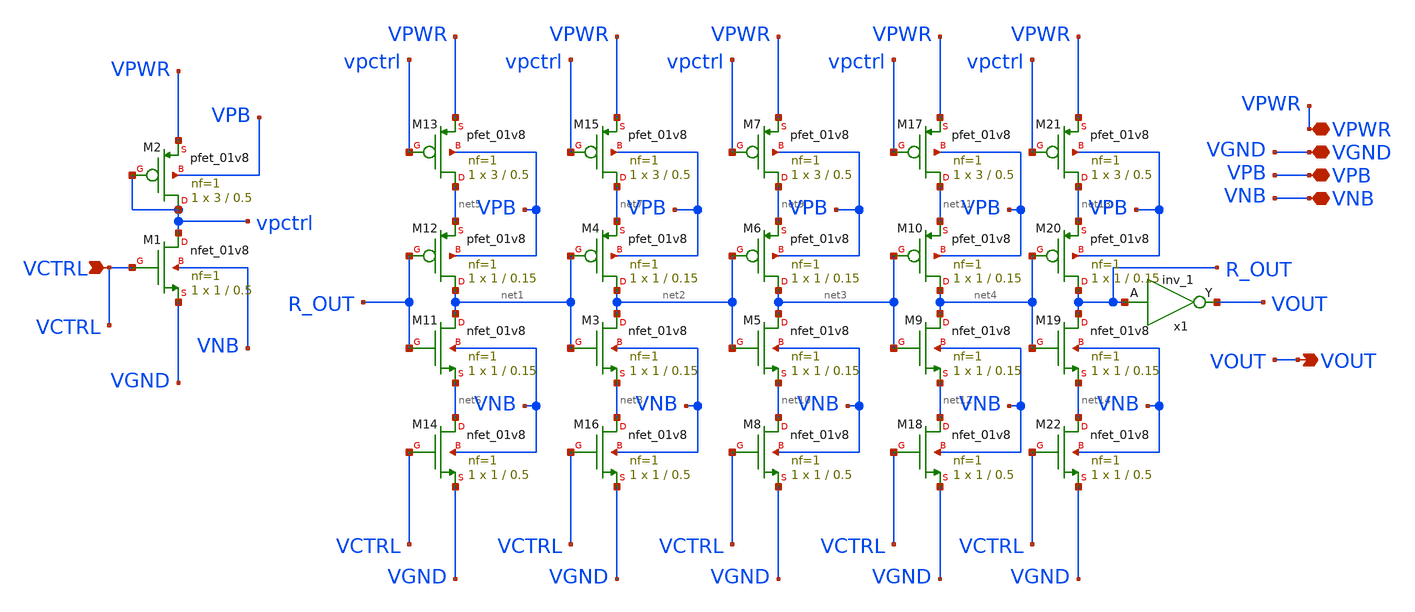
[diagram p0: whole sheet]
** sch_path: vco.sch
**.subckt vco VPWR VGND VPB VNB VOUT VCTRL
*.iopin VPWR
*.iopin VGND
*.iopin VPB
*.iopin VNB
*.opin VOUT
*.ipin VCTRL
XM1 vpctrl VCTRL VGND VNB sky130_fd_pr__nfet_01v8 L=0.5 W=1 nf=1 ad='int((1 + 1)/2) * 1 / 1 * 0.29' as='int((1 + 2)/2) * 1 / 1 * 0.29'
+ pd='2*int((1 + 1)/2) * (1 / 1 + 0.29)' ps='2*int((1 + 2)/2) * (1 / 1 + 0.29)' nrd='0.29 / 1 ' nrs='0.29 / 1 '
+ sa=0 sb=0 sd=0 mult=1 m=1
XM2 vpctrl vpctrl VPWR VPB sky130_fd_pr__pfet_01v8 L=0.5 W=3 nf=1 ad='int((1 + 1)/2) * 3 / 1 * 0.29'
+ as='int((1 + 2)/2) * 3 / 1 * 0.29' pd='2*int((1 + 1)/2) * (3 / 1 + 0.29)' ps='2*int((1 + 2)/2) * (3 / 1 + 0.29)'
+ nrd='0.29 / 3 ' nrs='0.29 / 3 ' sa=0 sb=0 sd=0 mult=1 m=1
XM11 net1 R_OUT net6 VNB sky130_fd_pr__nfet_01v8 L=0.15 W=1 nf=1 ad='int((1 + 1)/2) * 1 / 1 * 0.29' as='int((1 + 2)/2) * 1 / 1 * 0.29'
+ pd='2*int((1 + 1)/2) * (1 / 1 + 0.29)' ps='2*int((1 + 2)/2) * (1 / 1 + 0.29)' nrd='0.29 / 1 ' nrs='0.29 / 1 '
+ sa=0 sb=0 sd=0 mult=1 m=1
XM12 net1 R_OUT net5 VPB sky130_fd_pr__pfet_01v8 L=0.15 W=1 nf=1 ad='int((1 + 1)/2) * 1 / 1 * 0.29' as='int((1 + 2)/2) * 1 / 1 * 0.29'
+ pd='2*int((1 + 1)/2) * (1 / 1 + 0.29)' ps='2*int((1 + 2)/2) * (1 / 1 + 0.29)' nrd='0.29 / 1 ' nrs='0.29 / 1 '
+ sa=0 sb=0 sd=0 mult=1 m=1
XM13 net5 vpctrl VPWR VPB sky130_fd_pr__pfet_01v8 L=0.5 W=3 nf=1 ad='int((1 + 1)/2) * 3 / 1 * 0.29' as='int((1 + 2)/2) * 3 / 1 * 0.29'
+ pd='2*int((1 + 1)/2) * (3 / 1 + 0.29)' ps='2*int((1 + 2)/2) * (3 / 1 + 0.29)' nrd='0.29 / 3 ' nrs='0.29 / 3 '
+ sa=0 sb=0 sd=0 mult=1 m=1
XM14 net6 VCTRL VGND VNB sky130_fd_pr__nfet_01v8 L=0.5 W=1 nf=1 ad='int((1 + 1)/2) * 1 / 1 * 0.29' as='int((1 + 2)/2) * 1 / 1 * 0.29'
+ pd='2*int((1 + 1)/2) * (1 / 1 + 0.29)' ps='2*int((1 + 2)/2) * (1 / 1 + 0.29)' nrd='0.29 / 1 ' nrs='0.29 / 1 '
+ sa=0 sb=0 sd=0 mult=1 m=1
XM3 net2 net1 net8 VNB sky130_fd_pr__nfet_01v8 L=0.15 W=1 nf=1 ad='int((1 + 1)/2) * 1 / 1 * 0.29' as='int((1 + 2)/2) * 1 / 1 * 0.29'
+ pd='2*int((1 + 1)/2) * (1 / 1 + 0.29)' ps='2*int((1 + 2)/2) * (1 / 1 + 0.29)' nrd='0.29 / 1 ' nrs='0.29 / 1 '
+ sa=0 sb=0 sd=0 mult=1 m=1
XM4 net2 net1 net7 VPB sky130_fd_pr__pfet_01v8 L=0.15 W=1 nf=1 ad='int((1 + 1)/2) * 1 / 1 * 0.29' as='int((1 + 2)/2) * 1 / 1 * 0.29'
+ pd='2*int((1 + 1)/2) * (1 / 1 + 0.29)' ps='2*int((1 + 2)/2) * (1 / 1 + 0.29)' nrd='0.29 / 1 ' nrs='0.29 / 1 '
+ sa=0 sb=0 sd=0 mult=1 m=1
XM15 net7 vpctrl VPWR VPB sky130_fd_pr__pfet_01v8 L=0.5 W=3 nf=1 ad='int((1 + 1)/2) * 3 / 1 * 0.29' as='int((1 + 2)/2) * 3 / 1 * 0.29'
+ pd='2*int((1 + 1)/2) * (3 / 1 + 0.29)' ps='2*int((1 + 2)/2) * (3 / 1 + 0.29)' nrd='0.29 / 3 ' nrs='0.29 / 3 '
+ sa=0 sb=0 sd=0 mult=1 m=1
XM16 net8 VCTRL VGND VNB sky130_fd_pr__nfet_01v8 L=0.5 W=1 nf=1 ad='int((1 + 1)/2) * 1 / 1 * 0.29' as='int((1 + 2)/2) * 1 / 1 * 0.29'
+ pd='2*int((1 + 1)/2) * (1 / 1 + 0.29)' ps='2*int((1 + 2)/2) * (1 / 1 + 0.29)' nrd='0.29 / 1 ' nrs='0.29 / 1 '
+ sa=0 sb=0 sd=0 mult=1 m=1
XM5 net3 net2 net10 VNB sky130_fd_pr__nfet_01v8 L=0.15 W=1 nf=1 ad='int((1 + 1)/2) * 1 / 1 * 0.29' as='int((1 + 2)/2) * 1 / 1 * 0.29'
+ pd='2*int((1 + 1)/2) * (1 / 1 + 0.29)' ps='2*int((1 + 2)/2) * (1 / 1 + 0.29)' nrd='0.29 / 1 ' nrs='0.29 / 1 '
+ sa=0 sb=0 sd=0 mult=1 m=1
XM6 net3 net2 net9 VPB sky130_fd_pr__pfet_01v8 L=0.15 W=1 nf=1 ad='int((1 + 1)/2) * 1 / 1 * 0.29' as='int((1 + 2)/2) * 1 / 1 * 0.29'
+ pd='2*int((1 + 1)/2) * (1 / 1 + 0.29)' ps='2*int((1 + 2)/2) * (1 / 1 + 0.29)' nrd='0.29 / 1 ' nrs='0.29 / 1 '
+ sa=0 sb=0 sd=0 mult=1 m=1
XM7 net9 vpctrl VPWR VPB sky130_fd_pr__pfet_01v8 L=0.5 W=3 nf=1 ad='int((1 + 1)/2) * 3 / 1 * 0.29' as='int((1 + 2)/2) * 3 / 1 * 0.29'
+ pd='2*int((1 + 1)/2) * (3 / 1 + 0.29)' ps='2*int((1 + 2)/2) * (3 / 1 + 0.29)' nrd='0.29 / 3 ' nrs='0.29 / 3 '
+ sa=0 sb=0 sd=0 mult=1 m=1
XM8 net10 VCTRL VGND VNB sky130_fd_pr__nfet_01v8 L=0.5 W=1 nf=1 ad='int((1 + 1)/2) * 1 / 1 * 0.29' as='int((1 + 2)/2) * 1 / 1 * 0.29'
+ pd='2*int((1 + 1)/2) * (1 / 1 + 0.29)' ps='2*int((1 + 2)/2) * (1 / 1 + 0.29)' nrd='0.29 / 1 ' nrs='0.29 / 1 '
+ sa=0 sb=0 sd=0 mult=1 m=1
XM9 net4 net3 net12 VNB sky130_fd_pr__nfet_01v8 L=0.15 W=1 nf=1 ad='int((1 + 1)/2) * 1 / 1 * 0.29' as='int((1 + 2)/2) * 1 / 1 * 0.29'
+ pd='2*int((1 + 1)/2) * (1 / 1 + 0.29)' ps='2*int((1 + 2)/2) * (1 / 1 + 0.29)' nrd='0.29 / 1 ' nrs='0.29 / 1 '
+ sa=0 sb=0 sd=0 mult=1 m=1
XM10 net4 net3 net11 VPB sky130_fd_pr__pfet_01v8 L=0.15 W=1 nf=1 ad='int((1 + 1)/2) * 1 / 1 * 0.29' as='int((1 + 2)/2) * 1 / 1 * 0.29'
+ pd='2*int((1 + 1)/2) * (1 / 1 + 0.29)' ps='2*int((1 + 2)/2) * (1 / 1 + 0.29)' nrd='0.29 / 1 ' nrs='0.29 / 1 '
+ sa=0 sb=0 sd=0 mult=1 m=1
XM17 net11 vpctrl VPWR VPB sky130_fd_pr__pfet_01v8 L=0.5 W=3 nf=1 ad='int((1 + 1)/2) * 3 / 1 * 0.29'
+ as='int((1 + 2)/2) * 3 / 1 * 0.29' pd='2*int((1 + 1)/2) * (3 / 1 + 0.29)' ps='2*int((1 + 2)/2) * (3 / 1 + 0.29)'
+ nrd='0.29 / 3 ' nrs='0.29 / 3 ' sa=0 sb=0 sd=0 mult=1 m=1
XM18 net12 VCTRL VGND VNB sky130_fd_pr__nfet_01v8 L=0.5 W=1 nf=1 ad='int((1 + 1)/2) * 1 / 1 * 0.29' as='int((1 + 2)/2) * 1 / 1 * 0.29'
+ pd='2*int((1 + 1)/2) * (1 / 1 + 0.29)' ps='2*int((1 + 2)/2) * (1 / 1 + 0.29)' nrd='0.29 / 1 ' nrs='0.29 / 1 '
+ sa=0 sb=0 sd=0 mult=1 m=1
XM19 R_OUT net4 net14 VNB sky130_fd_pr__nfet_01v8 L=0.15 W=1 nf=1 ad='int((1 + 1)/2) * 1 / 1 * 0.29'
+ as='int((1 + 2)/2) * 1 / 1 * 0.29' pd='2*int((1 + 1)/2) * (1 / 1 + 0.29)' ps='2*int((1 + 2)/2) * (1 / 1 + 0.29)'
+ nrd='0.29 / 1 ' nrs='0.29 / 1 ' sa=0 sb=0 sd=0 mult=1 m=1
XM20 R_OUT net4 net13 VPB sky130_fd_pr__pfet_01v8 L=0.15 W=1 nf=1 ad='int((1 + 1)/2) * 1 / 1 * 0.29'
+ as='int((1 + 2)/2) * 1 / 1 * 0.29' pd='2*int((1 + 1)/2) * (1 / 1 + 0.29)' ps='2*int((1 + 2)/2) * (1 / 1 + 0.29)'
+ nrd='0.29 / 1 ' nrs='0.29 / 1 ' sa=0 sb=0 sd=0 mult=1 m=1
XM21 net13 vpctrl VPWR VPB sky130_fd_pr__pfet_01v8 L=0.5 W=3 nf=1 ad='int((1 + 1)/2) * 3 / 1 * 0.29'
+ as='int((1 + 2)/2) * 3 / 1 * 0.29' pd='2*int((1 + 1)/2) * (3 / 1 + 0.29)' ps='2*int((1 + 2)/2) * (3 / 1 + 0.29)'
+ nrd='0.29 / 3 ' nrs='0.29 / 3 ' sa=0 sb=0 sd=0 mult=1 m=1
XM22 net14 VCTRL VGND VNB sky130_fd_pr__nfet_01v8 L=0.5 W=1 nf=1 ad='int((1 + 1)/2) * 1 / 1 * 0.29' as='int((1 + 2)/2) * 1 / 1 * 0.29'
+ pd='2*int((1 + 1)/2) * (1 / 1 + 0.29)' ps='2*int((1 + 2)/2) * (1 / 1 + 0.29)' nrd='0.29 / 1 ' nrs='0.29 / 1 '
+ sa=0 sb=0 sd=0 mult=1 m=1
x1 R_OUT VGND VNB VPB VPWR VOUT sky130_fd_sc_hd__inv_1
**** begin user architecture code
OUT
**** end user architecture code
**.ends
.end
